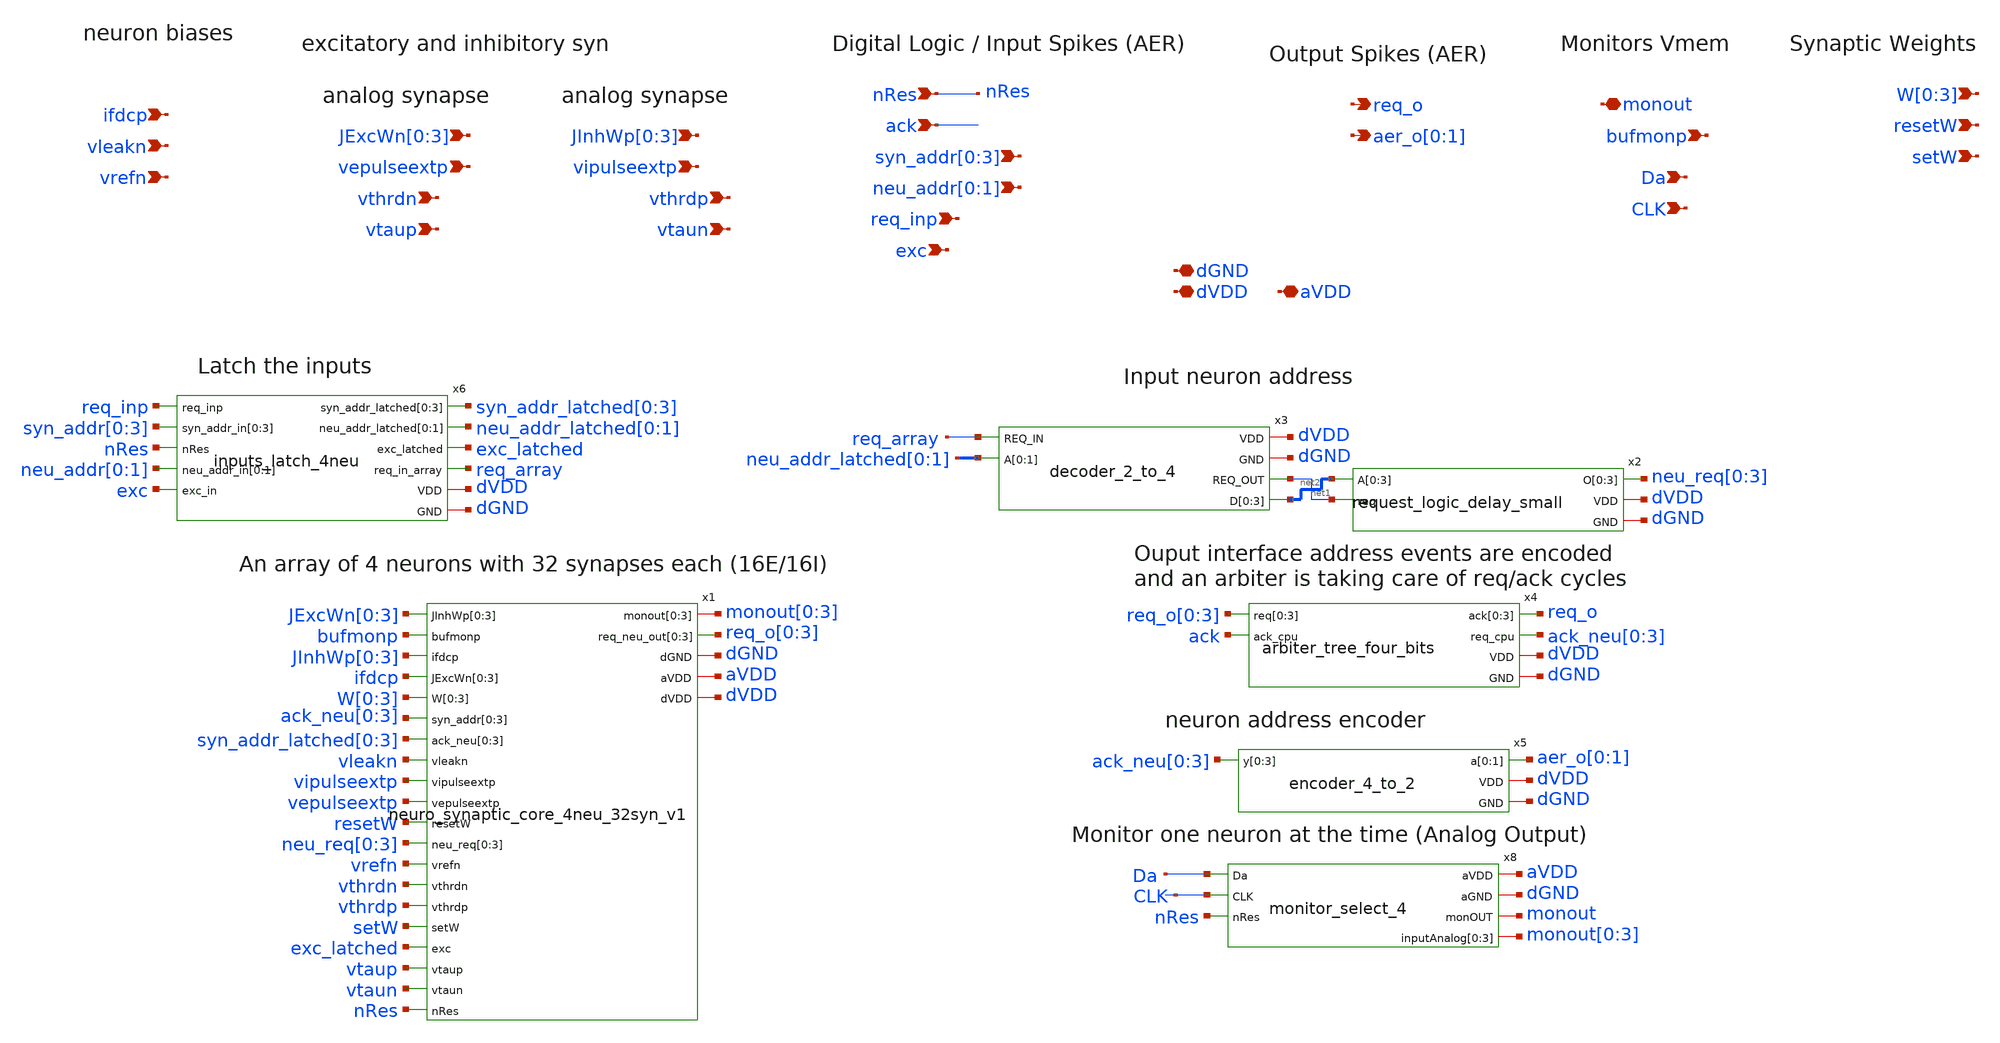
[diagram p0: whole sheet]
** sch_path: design/xschem/neuron_synapse_array_with_input_output_logic_v1_small.sch
**.subckt neuron_synapse_array_with_input_output_logic_v1_small vleakn vrefn ifdcp bufmonp req_o
*+ aer_o[0],aer_o[1] dGND dVDD nRes ack neu_addr[0],neu_addr[1] req_inp syn_addr[0],syn_addr[1],syn_addr[2],syn_addr[3]
*+ exc aVDD monout W[0],W[1],W[2],W[3] resetW setW vepulseextp vipulseextp
*+ JExcWn[0],JExcWn[1],JExcWn[2],JExcWn[3] JInhWp[0],JInhWp[1],JInhWp[2],JInhWp[3] vthrdp vtaun vthrdn vtaup Da CLK
*.ipin vleakn
*.ipin vrefn
*.ipin ifdcp
*.ipin bufmonp
*.opin req_o
*.opin aer_o[0],aer_o[1]
*.iopin dGND
*.iopin dVDD
*.ipin nRes
*.ipin ack
*.ipin neu_addr[0],neu_addr[1]
*.ipin req_inp
*.ipin syn_addr[0],syn_addr[1],syn_addr[2],syn_addr[3]
*.ipin exc
*.iopin aVDD
*.iopin monout
*.ipin W[0],W[1],W[2],W[3]
*.ipin resetW
*.ipin setW
*.ipin vepulseextp
*.ipin vipulseextp
*.ipin JExcWn[0],JExcWn[1],JExcWn[2],JExcWn[3]
*.ipin JInhWp[0],JInhWp[1],JInhWp[2],JInhWp[3]
*.ipin vthrdp
*.ipin vtaun
*.ipin vthrdn
*.ipin vtaup
*.ipin Da
*.ipin CLK
x1 JExcWn[0] JExcWn[1] JExcWn[2] JExcWn[3] bufmonp JInhWp[0] ifdcp ifdcp ifdcp ifdcp W[0] W[1] W[2]
+ W[3] ack_neu[0] ack_neu[1] ack_neu[2] ack_neu[3] syn_addr_latched[0] syn_addr_latched[1]
+ syn_addr_latched[2] syn_addr_latched[3] vleakn vipulseextp vepulseextp monout[0] monout[1] monout[2] monout[3] resetW
+ neu_req[0] neu_req[1] neu_req[2] neu_req[3] vrefn req_o[0] req_o[1] req_o[2] req_o[3] vthrdn vthrdp setW
+ exc_latched vtaup vtaun dGND aVDD dVDD nRes neuro_synaptic_core_4neu_32syn_v1
x3 dVDD dGND req_array net1 neu_addr_latched[0] neu_addr_latched[1] net2[3] net2[2] net2[1] net2[0]
+ decoder_2_to_4
x2 net2[3] net2[2] net2[1] net2[0] neu_req[0] neu_req[1] neu_req[2] neu_req[3] net1 dVDD dGND
+ request_logic_delay_small
x4 req_o[0] req_o[1] req_o[2] req_o[3] ack req_o req_o req_o req_o ack_neu[0] dVDD dGND
+ arbiter_tree_four_bits
x5 ack_neu[0] ack_neu[1] ack_neu[2] ack_neu[3] aer_o[0] aer_o[1] dVDD dGND encoder_4_to_2
x6 req_inp syn_addr_latched[0] syn_addr_latched[1] syn_addr_latched[2] syn_addr_latched[3]
+ syn_addr[0] syn_addr[1] syn_addr[2] syn_addr[3] nRes neu_addr_latched[0] neu_addr_latched[1] neu_addr[0]
+ neu_addr[1] exc_latched exc req_array dVDD dGND inputs_latch_4neu
x8 aVDD Da dGND CLK nRes monout monout[0] monout[1] monout[2] monout[3] monitor_select_4
**.ends
.end
